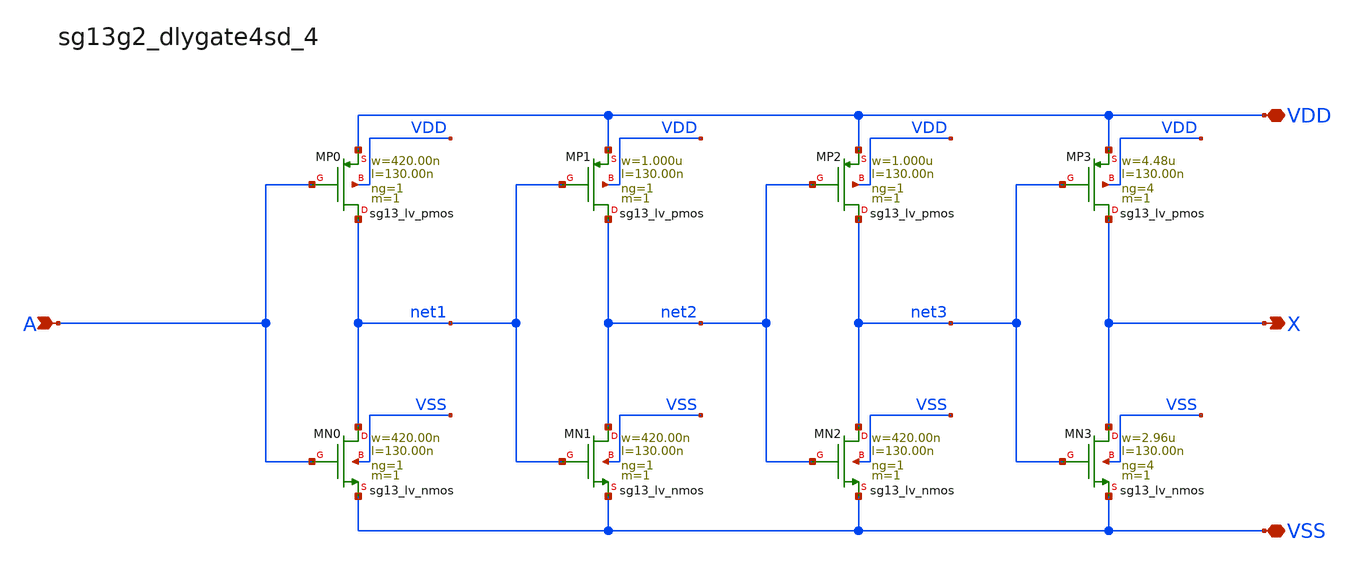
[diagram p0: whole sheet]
** sch_path: outputs/sg13g2_cells/cells/sg13g2_dlygate4sd_4/sg13g2_dlygate4sd_4.sch
**.subckt sg13g2_dlygate4sd_4 X A VDD VSS
*.opin X
*.ipin A
*.iopin VDD
*.iopin VSS
XMP3 X net3 VDD VDD sg13_lv_pmos w=4.48u l=130.00n ng=4 m=1 mm_ok=1
XMP2 net3 net2 VDD VDD sg13_lv_pmos w=1.000u l=130.00n ng=1 m=1 mm_ok=1
XMP1 net2 net1 VDD VDD sg13_lv_pmos w=1.000u l=130.00n ng=1 m=1 mm_ok=1
XMP0 net1 A VDD VDD sg13_lv_pmos w=420.00n l=130.00n ng=1 m=1 mm_ok=1
XMN3 X net3 VSS VSS sg13_lv_nmos w=2.96u l=130.00n ng=4 m=1 mm_ok=1
XMN2 net3 net2 VSS VSS sg13_lv_nmos w=420.00n l=130.00n ng=1 m=1 mm_ok=1
XMN1 net2 net1 VSS VSS sg13_lv_nmos w=420.00n l=130.00n ng=1 m=1 mm_ok=1
XMN0 net1 A VSS VSS sg13_lv_nmos w=420.00n l=130.00n ng=1 m=1 mm_ok=1
**.ends
.end
